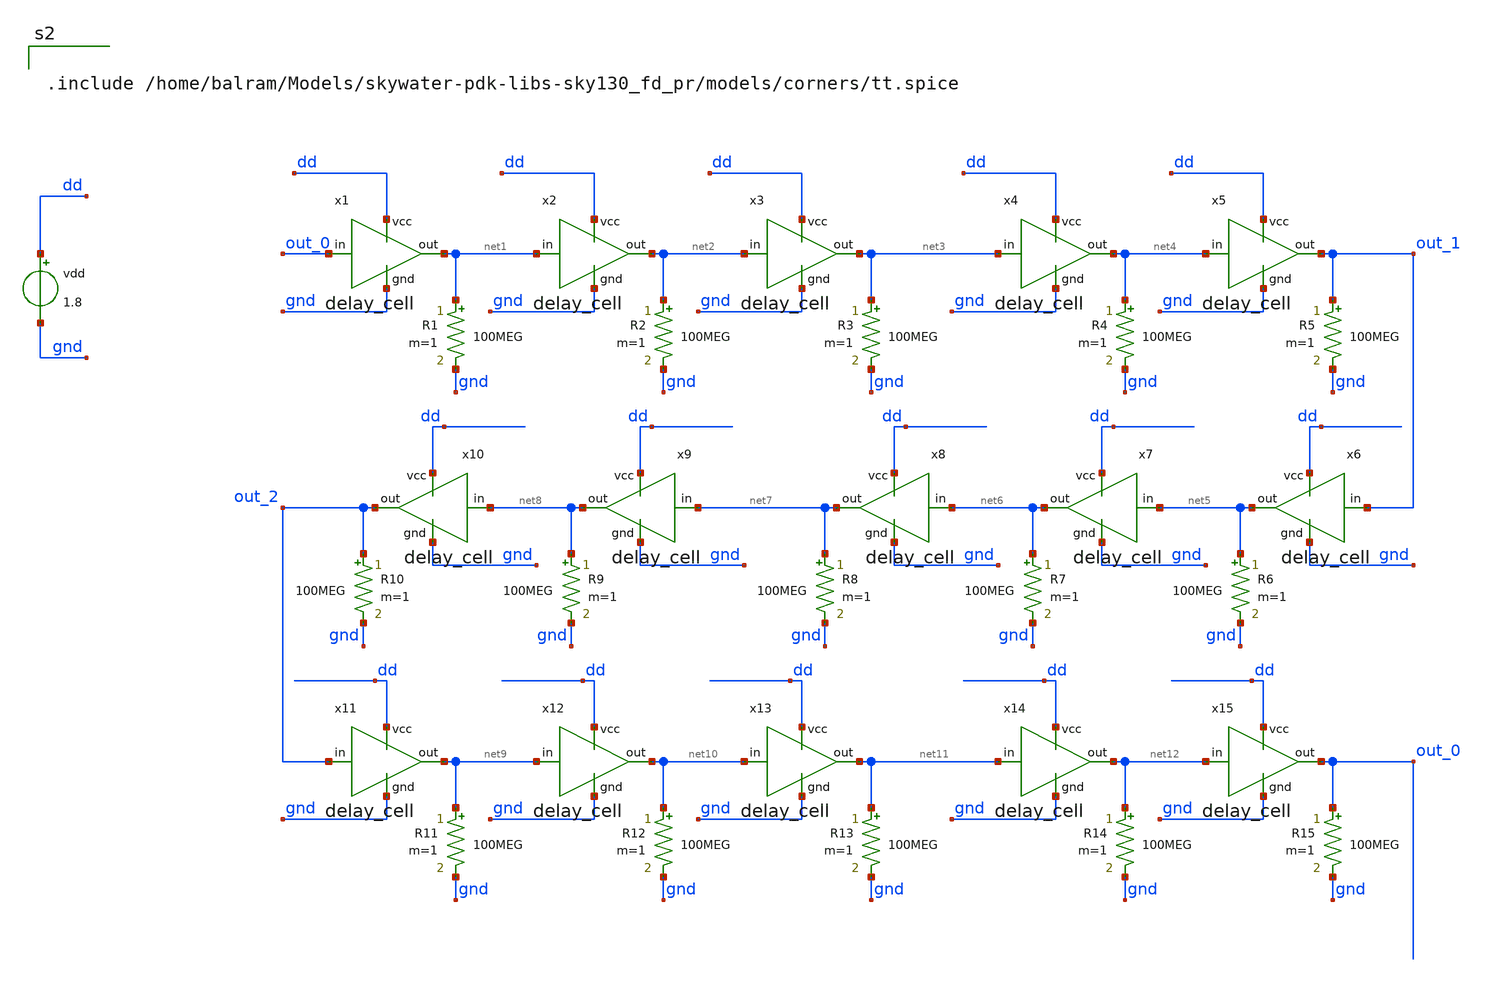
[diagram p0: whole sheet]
** sch_path: Oscillators/Ring-Oscillator/TB__oscillator.sch
**.subckt TB__oscillator
x1 dd out_0 net1 gnd delay_cell
vdd dd gnd 1.8
x2 dd net1 net2 gnd delay_cell
x3 dd net2 net3 gnd delay_cell
R1 net1 gnd 100MEG m=1
R2 net2 gnd 100MEG m=1
R3 net3 gnd 100MEG m=1
x4 dd net3 net4 gnd delay_cell
x5 dd net4 out_1 gnd delay_cell
R4 net4 gnd 100MEG m=1
R5 out_1 gnd 100MEG m=1
x6 dd out_1 net5 gnd delay_cell
x7 dd net5 net6 gnd delay_cell
x8 dd net6 net7 gnd delay_cell
R6 net5 gnd 100MEG m=1
R7 net6 gnd 100MEG m=1
R8 net7 gnd 100MEG m=1
x9 dd net7 net8 gnd delay_cell
x10 dd net8 out_2 gnd delay_cell
R9 net8 gnd 100MEG m=1
R10 out_2 gnd 100MEG m=1
x11 dd out_2 net9 gnd delay_cell
x12 dd net9 net10 gnd delay_cell
x13 dd net10 net11 gnd delay_cell
R11 net9 gnd 100MEG m=1
R12 net10 gnd 100MEG m=1
R13 net11 gnd 100MEG m=1
x14 dd net11 net12 gnd delay_cell
x15 dd net12 out_0 gnd delay_cell
R14 net12 gnd 100MEG m=1
R15 out_0 gnd 100MEG m=1
**** begin user architecture code


.include /home/balram/Models/skywater-pdk-libs-sky130_fd_pr/models/corners/tt.spice


**** end user architecture code
**.ends

* expanding   symbol:  delay_cell.sym # of pins=4
** sym_path: Oscillators/Ring-Oscillator/delay_cell.sym
** sch_path: Oscillators/Ring-Oscillator/delay_cell.sch
.subckt delay_cell vcc in out gnd
*.ipin vcc
*.ipin gnd
*.ipin in
*.opin out
XM1 out in gnd gnd sky130_fd_pr__nfet_01v8_lvt L=0.15 W=0.45 nf=1 ad='int((1 + 1)/2) * 0.45 / 1 * 0.29'
+ as='int((1 + 2)/2) * 0.45 / 1 * 0.29' pd='2*int((1 + 1)/2) * (0.45 / 1 + 0.29)' ps='2*int((1 + 2)/2) * (0.45 / 1 + 0.29)'
+ nrd='0.29 / 0.45 ' nrs='0.29 / 0.45 ' sa=0 sb=0 sd=0 mult=1 m=1
XM10 out in vcc vcc sky130_fd_pr__pfet_01v8_lvt L=0.35 W=0.45 nf=1 ad='int((1 + 1)/2) * 0.45 / 1 * 0.29'
+ as='int((1 + 2)/2) * 0.45 / 1 * 0.29' pd='2*int((1 + 1)/2) * (0.45 / 1 + 0.29)' ps='2*int((1 + 2)/2) * (0.45 / 1 + 0.29)'
+ nrd='0.29 / 0.45 ' nrs='0.29 / 0.45 ' sa=0 sb=0 sd=0 mult=1 m=1
.ends

.end
